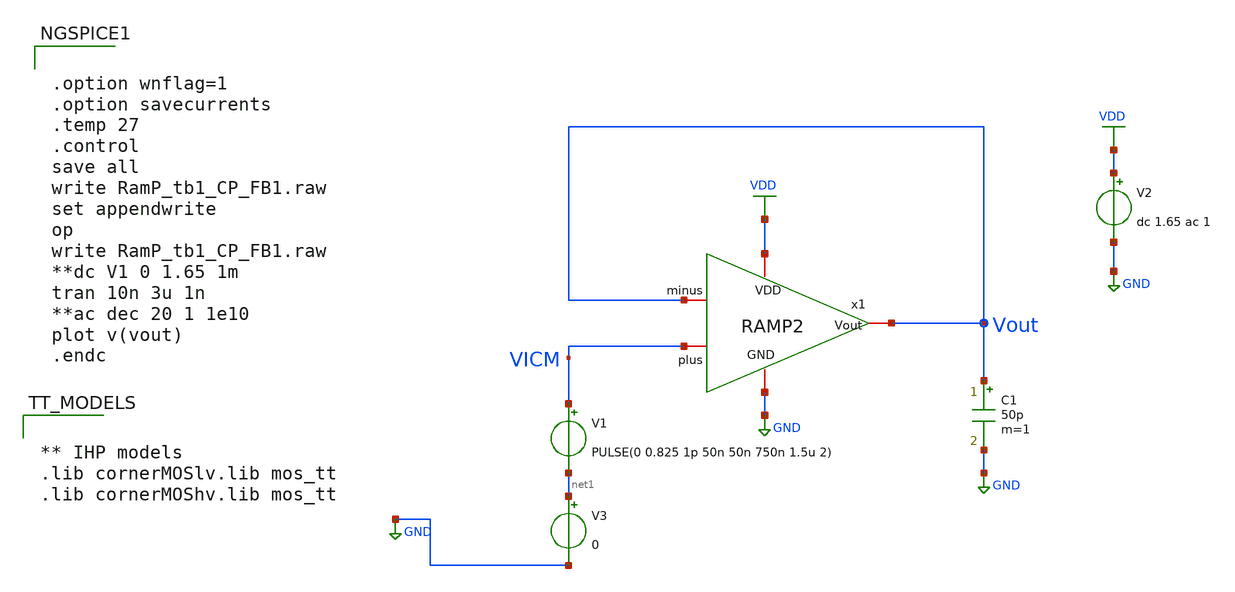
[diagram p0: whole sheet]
** sch_path: Design Files/RAMP/RAMP-Test/RamP_tb1_CP_FB1_1.sch
**.subckt RamP_tb1_CP_FB1_1
V2 VDD GND dc 1.65 ac 1
C1 Vout GND 50p m=1
x1 VDD VICM Vout Vout GND RAMP2
V1 VICM net1 PULSE(0 0.825 1p 50n 50n 750n 1.5u 2)
V3 net1 GND 0
**** begin user architecture code


** IHP models
.lib cornerMOSlv.lib mos_tt
.lib cornerMOShv.lib mos_tt




.save @n.x1.x2.xmn_stg2_3n1.nsg13_lv_nmos[gm]
.save @n.x1.x2.xmn_stg2_3n1.nsg13_lv_nmos[gds]
.save @n.x1.x2.xmn_stg2_3n1.nsg13_lv_nmos[vth]
.save @n.x1.x2.xmn_stg2_3n1.nsg13_lv_nmos[vdss]
.save @n.x1.x2.xmn_stg2_3n1.nsg13_lv_nmos[cgg]
.save @n.x1.x2.xmn_stg2_3n1.nsg13_lv_nmos[cgsol]
.save @n.x1.x2.xmn_stg2_3n1.nsg13_lv_nmos[cgdol]
.save @n.x1.x2.xmn_stg2_3p1.nsg13_lv_pmos[gm]
.save @n.x1.x2.xmn_stg2_3p1.nsg13_lv_pmos[gds]
.save @n.x1.x2.xmn_stg2_3p1.nsg13_lv_pmos[vth]
.save @n.x1.x2.xmn_stg2_3p1.nsg13_lv_pmos[vdss]
.save @n.x1.x2.xmn_stg2_3p1.nsg13_lv_pmos[cgg]
.save @n.x1.x2.xmn_stg2_3p1.nsg13_lv_pmos[cgsol]
.save @n.x1.x2.xmn_stg2_3p1.nsg13_lv_pmos[cgdol]
.save @n.x1.x2.xmp_dz_stg2_3n.nsg13_lv_pmos[gm]
.save @n.x1.x2.xmp_dz_stg2_3n.nsg13_lv_pmos[gds]
.save @n.x1.x2.xmp_dz_stg2_3n.nsg13_lv_pmos[vth]
.save @n.x1.x2.xmp_dz_stg2_3n.nsg13_lv_pmos[vdss]
.save @n.x1.x2.xmp_dz_stg2_3n.nsg13_lv_pmos[cgg]
.save @n.x1.x2.xmp_dz_stg2_3n.nsg13_lv_pmos[cgsol]
.save @n.x1.x2.xmp_dz_stg2_3n.nsg13_lv_pmos[cgdol]
.save @n.x1.x2.xmp_stg2_3p2.nsg13_lv_nmos[gm]
.save @n.x1.x2.xmp_stg2_3p2.nsg13_lv_nmos[gds]
.save @n.x1.x2.xmp_stg2_3p2.nsg13_lv_nmos[vth]
.save @n.x1.x2.xmp_stg2_3p2.nsg13_lv_nmos[vdss]
.save @n.x1.x2.xmp_stg2_3p2.nsg13_lv_nmos[cgg]
.save @n.x1.x2.xmp_stg2_3p2.nsg13_lv_nmos[cgsol]
.save @n.x1.x2.xmp_stg2_3p2.nsg13_lv_nmos[cgdol]
.save @n.x1.x2.xmp_stg2_3p1.nsg13_lv_pmos[gm]
.save @n.x1.x2.xmp_stg2_3p1.nsg13_lv_pmos[gds]
.save @n.x1.x2.xmp_stg2_3p1.nsg13_lv_pmos[vth]
.save @n.x1.x2.xmp_stg2_3p1.nsg13_lv_pmos[vdss]
.save @n.x1.x2.xmp_stg2_3p1.nsg13_lv_pmos[cgg]
.save @n.x1.x2.xmp_stg2_3p1.nsg13_lv_pmos[cgsol]
.save @n.x1.x2.xmp_stg2_3p1.nsg13_lv_pmos[cgdol]
.save @n.x1.x2.xmn_dz_stg2_3p.nsg13_lv_nmos[gm]
.save @n.x1.x2.xmn_dz_stg2_3p.nsg13_lv_nmos[gds]
.save @n.x1.x2.xmn_dz_stg2_3p.nsg13_lv_nmos[vth]
.save @n.x1.x2.xmn_dz_stg2_3p.nsg13_lv_nmos[vdss]
.save @n.x1.x2.xmn_dz_stg2_3p.nsg13_lv_nmos[cgg]
.save @n.x1.x2.xmn_dz_stg2_3p.nsg13_lv_nmos[cgsol]
.save @n.x1.x2.xmn_dz_stg2_3p.nsg13_lv_nmos[cgdol]
.save @n.x1.xm1.nsg13_hv_nmos[gm]
.save @n.x1.xm1.nsg13_hv_nmos[gds]
.save @n.x1.xm1.nsg13_hv_nmos[vth]
.save @n.x1.xm1.nsg13_hv_nmos[vdss]
.save @n.x1.xm1.nsg13_hv_nmos[cgg]
.save @n.x1.xm1.nsg13_hv_nmos[cgsol]
.save @n.x1.xm1.nsg13_hv_nmos[cgdol]
.save @n.x1.xm2.nsg13_hv_pmos[gm]
.save @n.x1.xm2.nsg13_hv_pmos[gds]
.save @n.x1.xm2.nsg13_hv_pmos[vth]
.save @n.x1.xm2.nsg13_hv_pmos[vdss]
.save @n.x1.xm2.nsg13_hv_pmos[cgg]
.save @n.x1.xm2.nsg13_hv_pmos[cgsol]
.save @n.x1.xm2.nsg13_hv_pmos[cgdol]
.save @n.x1.x3.xmn_stg2_3n1.nsg13_lv_nmos[gm]
.save @n.x1.x3.xmn_stg2_3n1.nsg13_lv_nmos[gds]
.save @n.x1.x3.xmn_stg2_3n1.nsg13_lv_nmos[vth]
.save @n.x1.x3.xmn_stg2_3n1.nsg13_lv_nmos[vdss]
.save @n.x1.x3.xmn_stg2_3n1.nsg13_lv_nmos[cgg]
.save @n.x1.x3.xmn_stg2_3n1.nsg13_lv_nmos[cgsol]
.save @n.x1.x3.xmn_stg2_3n1.nsg13_lv_nmos[cgdol]
.save @n.x1.x3.xmn_stg2_3p1.nsg13_lv_pmos[gm]
.save @n.x1.x3.xmn_stg2_3p1.nsg13_lv_pmos[gds]
.save @n.x1.x3.xmn_stg2_3p1.nsg13_lv_pmos[vth]
.save @n.x1.x3.xmn_stg2_3p1.nsg13_lv_pmos[vdss]
.save @n.x1.x3.xmn_stg2_3p1.nsg13_lv_pmos[cgg]
.save @n.x1.x3.xmn_stg2_3p1.nsg13_lv_pmos[cgsol]
.save @n.x1.x3.xmn_stg2_3p1.nsg13_lv_pmos[cgdol]
.save @n.x1.x3.xmp_dz_stg2_3n.nsg13_lv_pmos[gm]
.save @n.x1.x3.xmp_dz_stg2_3n.nsg13_lv_pmos[gds]
.save @n.x1.x3.xmp_dz_stg2_3n.nsg13_lv_pmos[vth]
.save @n.x1.x3.xmp_dz_stg2_3n.nsg13_lv_pmos[vdss]
.save @n.x1.x3.xmp_dz_stg2_3n.nsg13_lv_pmos[cgg]
.save @n.x1.x3.xmp_dz_stg2_3n.nsg13_lv_pmos[cgsol]
.save @n.x1.x3.xmp_dz_stg2_3n.nsg13_lv_pmos[cgdol]
.save @n.x1.x3.xmp_stg2_3p2.nsg13_lv_nmos[gm]
.save @n.x1.x3.xmp_stg2_3p2.nsg13_lv_nmos[gds]
.save @n.x1.x3.xmp_stg2_3p2.nsg13_lv_nmos[vth]
.save @n.x1.x3.xmp_stg2_3p2.nsg13_lv_nmos[vdss]
.save @n.x1.x3.xmp_stg2_3p2.nsg13_lv_nmos[cgg]
.save @n.x1.x3.xmp_stg2_3p2.nsg13_lv_nmos[cgsol]
.save @n.x1.x3.xmp_stg2_3p2.nsg13_lv_nmos[cgdol]
.save @n.x1.x3.xmp_stg2_3p1.nsg13_lv_pmos[gm]
.save @n.x1.x3.xmp_stg2_3p1.nsg13_lv_pmos[gds]
.save @n.x1.x3.xmp_stg2_3p1.nsg13_lv_pmos[vth]
.save @n.x1.x3.xmp_stg2_3p1.nsg13_lv_pmos[vdss]
.save @n.x1.x3.xmp_stg2_3p1.nsg13_lv_pmos[cgg]
.save @n.x1.x3.xmp_stg2_3p1.nsg13_lv_pmos[cgsol]
.save @n.x1.x3.xmp_stg2_3p1.nsg13_lv_pmos[cgdol]
.save @n.x1.x3.xmn_dz_stg2_3p.nsg13_lv_nmos[gm]
.save @n.x1.x3.xmn_dz_stg2_3p.nsg13_lv_nmos[gds]
.save @n.x1.x3.xmn_dz_stg2_3p.nsg13_lv_nmos[vth]
.save @n.x1.x3.xmn_dz_stg2_3p.nsg13_lv_nmos[vdss]
.save @n.x1.x3.xmn_dz_stg2_3p.nsg13_lv_nmos[cgg]
.save @n.x1.x3.xmn_dz_stg2_3p.nsg13_lv_nmos[cgsol]
.save @n.x1.x3.xmn_dz_stg2_3p.nsg13_lv_nmos[cgdol]
.save @n.x1.x3.xmn_stg2_3n_r.nsg13_hv_nmos[gm]
.save @n.x1.x3.xmn_stg2_3n_r.nsg13_hv_nmos[gds]
.save @n.x1.x3.xmn_stg2_3n_r.nsg13_hv_nmos[vth]
.save @n.x1.x3.xmn_stg2_3n_r.nsg13_hv_nmos[vdss]
.save @n.x1.x3.xmn_stg2_3n_r.nsg13_hv_nmos[cgg]
.save @n.x1.x3.xmn_stg2_3n_r.nsg13_hv_nmos[cgsol]
.save @n.x1.x3.xmn_stg2_3n_r.nsg13_hv_nmos[cgdol]
.save @n.x1.x3.x1.xm2.nsg13_lv_pmos[gm]
.save @n.x1.x3.x1.xm2.nsg13_lv_pmos[gds]
.save @n.x1.x3.x1.xm2.nsg13_lv_pmos[vth]
.save @n.x1.x3.x1.xm2.nsg13_lv_pmos[vdss]
.save @n.x1.x3.x1.xm2.nsg13_lv_pmos[cgg]
.save @n.x1.x3.x1.xm2.nsg13_lv_pmos[cgsol]
.save @n.x1.x3.x1.xm2.nsg13_lv_pmos[cgdol]
.save @n.x1.x3.x1.xm4.nsg13_hv_nmos[gm]
.save @n.x1.x3.x1.xm4.nsg13_hv_nmos[gds]
.save @n.x1.x3.x1.xm4.nsg13_hv_nmos[vth]
.save @n.x1.x3.x1.xm4.nsg13_hv_nmos[vdss]
.save @n.x1.x3.x1.xm4.nsg13_hv_nmos[cgg]
.save @n.x1.x3.x1.xm4.nsg13_hv_nmos[cgsol]
.save @n.x1.x3.x1.xm4.nsg13_hv_nmos[cgdol]
.save @n.x1.x3.x1.xm5.nsg13_hv_nmos[gm]
.save @n.x1.x3.x1.xm5.nsg13_hv_nmos[gds]
.save @n.x1.x3.x1.xm5.nsg13_hv_nmos[vth]
.save @n.x1.x3.x1.xm5.nsg13_hv_nmos[vdss]
.save @n.x1.x3.x1.xm5.nsg13_hv_nmos[cgg]
.save @n.x1.x3.x1.xm5.nsg13_hv_nmos[cgsol]
.save @n.x1.x3.x1.xm5.nsg13_hv_nmos[cgdol]
.save @n.x1.x3.x1.xm1.nsg13_lv_pmos[gm]
.save @n.x1.x3.x1.xm1.nsg13_lv_pmos[gds]
.save @n.x1.x3.x1.xm1.nsg13_lv_pmos[vth]
.save @n.x1.x3.x1.xm1.nsg13_lv_pmos[vdss]
.save @n.x1.x3.x1.xm1.nsg13_lv_pmos[cgg]
.save @n.x1.x3.x1.xm1.nsg13_lv_pmos[cgsol]
.save @n.x1.x3.x1.xm1.nsg13_lv_pmos[cgdol]
.save @n.x1.x3.xmp_stg2_3p_r.nsg13_hv_pmos[gm]
.save @n.x1.x3.xmp_stg2_3p_r.nsg13_hv_pmos[gds]
.save @n.x1.x3.xmp_stg2_3p_r.nsg13_hv_pmos[vth]
.save @n.x1.x3.xmp_stg2_3p_r.nsg13_hv_pmos[vdss]
.save @n.x1.x3.xmp_stg2_3p_r.nsg13_hv_pmos[cgg]
.save @n.x1.x3.xmp_stg2_3p_r.nsg13_hv_pmos[cgsol]
.save @n.x1.x3.xmp_stg2_3p_r.nsg13_hv_pmos[cgdol]
.save @n.x1.x3.x2.xm1.nsg13_hv_nmos[gm]
.save @n.x1.x3.x2.xm1.nsg13_hv_nmos[gds]
.save @n.x1.x3.x2.xm1.nsg13_hv_nmos[vth]
.save @n.x1.x3.x2.xm1.nsg13_hv_nmos[vdss]
.save @n.x1.x3.x2.xm1.nsg13_hv_nmos[cgg]
.save @n.x1.x3.x2.xm1.nsg13_hv_nmos[cgsol]
.save @n.x1.x3.x2.xm1.nsg13_hv_nmos[cgdol]
.save @n.x1.x3.x2.xm2.nsg13_hv_nmos[gm]
.save @n.x1.x3.x2.xm2.nsg13_hv_nmos[gds]
.save @n.x1.x3.x2.xm2.nsg13_hv_nmos[vth]
.save @n.x1.x3.x2.xm2.nsg13_hv_nmos[vdss]
.save @n.x1.x3.x2.xm2.nsg13_hv_nmos[cgg]
.save @n.x1.x3.x2.xm2.nsg13_hv_nmos[cgsol]
.save @n.x1.x3.x2.xm2.nsg13_hv_nmos[cgdol]
.save @n.x1.x3.x2.xm3.nsg13_hv_pmos[gm]
.save @n.x1.x3.x2.xm3.nsg13_hv_pmos[gds]
.save @n.x1.x3.x2.xm3.nsg13_hv_pmos[vth]
.save @n.x1.x3.x2.xm3.nsg13_hv_pmos[vdss]
.save @n.x1.x3.x2.xm3.nsg13_hv_pmos[cgg]
.save @n.x1.x3.x2.xm3.nsg13_hv_pmos[cgsol]
.save @n.x1.x3.x2.xm3.nsg13_hv_pmos[cgdol]
.save @n.x1.x3.x2.xm4.nsg13_hv_pmos[gm]
.save @n.x1.x3.x2.xm4.nsg13_hv_pmos[gds]
.save @n.x1.x3.x2.xm4.nsg13_hv_pmos[vth]
.save @n.x1.x3.x2.xm4.nsg13_hv_pmos[vdss]
.save @n.x1.x3.x2.xm4.nsg13_hv_pmos[cgg]
.save @n.x1.x3.x2.xm4.nsg13_hv_pmos[cgsol]
.save @n.x1.x3.x2.xm4.nsg13_hv_pmos[cgdol]
.save @n.x1.x4.xm9.nsg13_lv_nmos[gm]
.save @n.x1.x4.xm9.nsg13_lv_nmos[gds]
.save @n.x1.x4.xm9.nsg13_lv_nmos[vth]
.save @n.x1.x4.xm9.nsg13_lv_nmos[vdss]
.save @n.x1.x4.xm9.nsg13_lv_nmos[cgg]
.save @n.x1.x4.xm9.nsg13_lv_nmos[cgsol]
.save @n.x1.x4.xm9.nsg13_lv_nmos[cgdol]
.save @n.x1.x4.xm10.nsg13_lv_pmos[gm]
.save @n.x1.x4.xm10.nsg13_lv_pmos[gds]
.save @n.x1.x4.xm10.nsg13_lv_pmos[vth]
.save @n.x1.x4.xm10.nsg13_lv_pmos[vdss]
.save @n.x1.x4.xm10.nsg13_lv_pmos[cgg]
.save @n.x1.x4.xm10.nsg13_lv_pmos[cgsol]
.save @n.x1.x4.xm10.nsg13_lv_pmos[cgdol]
.save @n.x1.x4.xm11.nsg13_lv_pmos[gm]
.save @n.x1.x4.xm11.nsg13_lv_pmos[gds]
.save @n.x1.x4.xm11.nsg13_lv_pmos[vth]
.save @n.x1.x4.xm11.nsg13_lv_pmos[vdss]
.save @n.x1.x4.xm11.nsg13_lv_pmos[cgg]
.save @n.x1.x4.xm11.nsg13_lv_pmos[cgsol]
.save @n.x1.x4.xm11.nsg13_lv_pmos[cgdol]
.save @n.x1.x4.xm12.nsg13_lv_nmos[gm]
.save @n.x1.x4.xm12.nsg13_lv_nmos[gds]
.save @n.x1.x4.xm12.nsg13_lv_nmos[vth]
.save @n.x1.x4.xm12.nsg13_lv_nmos[vdss]
.save @n.x1.x4.xm12.nsg13_lv_nmos[cgg]
.save @n.x1.x4.xm12.nsg13_lv_nmos[cgsol]
.save @n.x1.x4.xm12.nsg13_lv_nmos[cgdol]
.save @n.x1.x4.xm13.nsg13_lv_pmos[gm]
.save @n.x1.x4.xm13.nsg13_lv_pmos[gds]
.save @n.x1.x4.xm13.nsg13_lv_pmos[vth]
.save @n.x1.x4.xm13.nsg13_lv_pmos[vdss]
.save @n.x1.x4.xm13.nsg13_lv_pmos[cgg]
.save @n.x1.x4.xm13.nsg13_lv_pmos[cgsol]
.save @n.x1.x4.xm13.nsg13_lv_pmos[cgdol]
.save @n.x1.x4.xm14.nsg13_lv_nmos[gm]
.save @n.x1.x4.xm14.nsg13_lv_nmos[gds]
.save @n.x1.x4.xm14.nsg13_lv_nmos[vth]
.save @n.x1.x4.xm14.nsg13_lv_nmos[vdss]
.save @n.x1.x4.xm14.nsg13_lv_nmos[cgg]
.save @n.x1.x4.xm14.nsg13_lv_nmos[cgsol]
.save @n.x1.x4.xm14.nsg13_lv_nmos[cgdol]
.save @n.x1.x5.xmn_stg1_ip_n1.nsg13_lv_nmos[gm]
.save @n.x1.x5.xmn_stg1_ip_n1.nsg13_lv_nmos[gds]
.save @n.x1.x5.xmn_stg1_ip_n1.nsg13_lv_nmos[vth]
.save @n.x1.x5.xmn_stg1_ip_n1.nsg13_lv_nmos[vdss]
.save @n.x1.x5.xmn_stg1_ip_n1.nsg13_lv_nmos[cgg]
.save @n.x1.x5.xmn_stg1_ip_n1.nsg13_lv_nmos[cgsol]
.save @n.x1.x5.xmn_stg1_ip_n1.nsg13_lv_nmos[cgdol]
.save @n.x1.x5.xmn_stg1_ip_n2.nsg13_lv_nmos[gm]
.save @n.x1.x5.xmn_stg1_ip_n2.nsg13_lv_nmos[gds]
.save @n.x1.x5.xmn_stg1_ip_n2.nsg13_lv_nmos[vth]
.save @n.x1.x5.xmn_stg1_ip_n2.nsg13_lv_nmos[vdss]
.save @n.x1.x5.xmn_stg1_ip_n2.nsg13_lv_nmos[cgg]
.save @n.x1.x5.xmn_stg1_ip_n2.nsg13_lv_nmos[cgsol]
.save @n.x1.x5.xmn_stg1_ip_n2.nsg13_lv_nmos[cgdol]
.save @n.x1.x5.xmp_stg1_cl_p1.nsg13_hv_pmos[gm]
.save @n.x1.x5.xmp_stg1_cl_p1.nsg13_hv_pmos[gds]
.save @n.x1.x5.xmp_stg1_cl_p1.nsg13_hv_pmos[vth]
.save @n.x1.x5.xmp_stg1_cl_p1.nsg13_hv_pmos[vdss]
.save @n.x1.x5.xmp_stg1_cl_p1.nsg13_hv_pmos[cgg]
.save @n.x1.x5.xmp_stg1_cl_p1.nsg13_hv_pmos[cgsol]
.save @n.x1.x5.xmp_stg1_cl_p1.nsg13_hv_pmos[cgdol]
.save @n.x1.x5.xmp_stg1_cl_p2.nsg13_hv_pmos[gm]
.save @n.x1.x5.xmp_stg1_cl_p2.nsg13_hv_pmos[gds]
.save @n.x1.x5.xmp_stg1_cl_p2.nsg13_hv_pmos[vth]
.save @n.x1.x5.xmp_stg1_cl_p2.nsg13_hv_pmos[vdss]
.save @n.x1.x5.xmp_stg1_cl_p2.nsg13_hv_pmos[cgg]
.save @n.x1.x5.xmp_stg1_cl_p2.nsg13_hv_pmos[cgsol]
.save @n.x1.x5.xmp_stg1_cl_p2.nsg13_hv_pmos[cgdol]



.option wnflag=1
.option savecurrents
.temp 27
.control
save all
write RamP_tb1_CP_FB1.raw
set appendwrite
op
write RamP_tb1_CP_FB1.raw
**dc V1 0 1.65 1m
tran 10n 3u 1n
**ac dec 20 1 1e10
plot v(vout)
.endc


**** end user architecture code
**.ends

* expanding   symbol:  /foss/designs/RAMP/Fully-Diff-RAMP/RAMP2.sym # of pins=5
** sym_path: Design Files/RAMP/Fully-Diff-RAMP/RAMP2.sym
** sch_path: Design Files/RAMP/Fully-Diff-RAMP/RAMP2.sch
.subckt RAMP2 VDD plus Vout minus GND
*.iopin GND
*.iopin plus
*.iopin minus
*.iopin Vout
*.iopin VDD
x2 VDD net2 mp_dz Vo_STG1 mn_dz net1 GND STG2
XM1 Vout mn_dz GND GND sg13_hv_nmos w=2.3u l=1u ng=1 m=4 mm_ok=1
XM2 Vout mp_dz VDD VDD sg13_hv_pmos w=4.5u l=0.5u ng=1 m=4 mm_ok=1
x3 VDD net2 V1_CM net1 GND STG2_Replica
x4 VDD V1_CM GND STG1-CM
x5 VDD Vo_STG1 plus minus V1_CM GND STG1_2
.ends


* expanding   symbol:  Fully-Diff-RAMP/STG2.sym # of pins=7
** sym_path: Design Files/RAMP/Fully-Diff-RAMP/STG2.sym
** sch_path: Design Files/RAMP/Fully-Diff-RAMP/STG2.sch
.subckt STG2 VDD VCTRL_P VDZP Vin_2 VDZN VCTRL_N GND
*.ipin Vin_2
*.ipin VDD
*.ipin GND
*.ipin VCTRL_P
*.ipin VCTRL_N
*.opin VDZN
*.opin VDZP
XMN_STG2_3N1 VDZN Vin_2 GND GND sg13_lv_nmos w=0.15u l=0.13u ng=1 m=1 mm_ok=1
XMN_STG2_3P1 VDZN Vin_2 net1 VDD sg13_lv_pmos w=0.15u l=0.13u ng=1 m=3 mm_ok=1
XMP_DZ_STG2_3N net1 VCTRL_P VDD VDD sg13_lv_pmos w=0.15u l=0.13u ng=1 m=5 mm_ok=1
XMP_STG2_3P2 VDZP Vin_2 net2 net2 sg13_lv_nmos w=0.15u l=0.13u ng=1 m=1 mm_ok=1
XMP_STG2_3P1 VDZP Vin_2 VDD VDD sg13_lv_pmos w=0.15u l=0.13u ng=1 m=1 mm_ok=1
XMN_DZ_STG2_3P net2 VCTRL_N GND GND sg13_lv_nmos w=0.15u l=0.13u ng=1 m=1 mm_ok=1
.ends


* expanding   symbol:  Fully-Diff-RAMP/STG2_Replica.sym # of pins=5
** sym_path: Design Files/RAMP/Fully-Diff-RAMP/STG2_Replica.sym
** sch_path: Design Files/RAMP/Fully-Diff-RAMP/STG2_Replica.sch
.subckt STG2_Replica VDD VCTRLP Vin_STG2 VCTRLN GND
*.ipin Vin_STG2
*.iopin VDD
*.iopin GND
*.opin VCTRLP
*.opin VCTRLN
XMN_STG2_3N1 net1 Vin_STG2 GND GND sg13_lv_nmos w=0.15u l=0.13u ng=1 m=1 mm_ok=1
XMN_STG2_3P1 net1 Vin_STG2 net2 VDD sg13_lv_pmos w=0.15u l=0.13u ng=1 m=3 mm_ok=1
XMP_DZ_STG2_3N net2 VCTRLP VDD VDD sg13_lv_pmos w=0.15u l=0.13u ng=1 m=5 mm_ok=1
XMP_STG2_3P2 net4 Vin_STG2 net3 net3 sg13_lv_nmos w=0.15u l=0.13u ng=1 m=1 mm_ok=1
XMP_STG2_3P1 net4 Vin_STG2 VDD VDD sg13_lv_pmos w=0.15u l=0.13u ng=1 m=1 mm_ok=1
XMN_DZ_STG2_3P net3 VCTRLN GND GND sg13_lv_nmos w=0.15u l=0.13u ng=1 m=1 mm_ok=1
XMN_STG2_3N_R net5 net5 GND GND sg13_hv_nmos w=2.3u l=1u ng=1 m=1 mm_ok=1
I0 VDD net5 1u
x1 VDD net1 net5 VCTRLP GND POTA
XMP_STG2_3P_R net6 net6 VDD VDD sg13_hv_pmos w=4.5u l=0.5u ng=1 m=1 mm_ok=1
I1 net6 GND 1u
x2 VDD VCTRLN net4 net6 GND NOTA
.ends


* expanding   symbol:  Fully-Diff-RAMP/STG1-CM.sym # of pins=3
** sym_path: Design Files/RAMP/Fully-Diff-RAMP/STG1-CM.sym
** sch_path: Design Files/RAMP/Fully-Diff-RAMP/STG1-CM.sch
.subckt STG1-CM VDD V_CM1 GND
*.ipin VDD
*.ipin GND
*.opin V_CM1
XM9 V_CM1 V_CM1 GND GND sg13_lv_nmos w=0.15u l=0.13u ng=1 m=1 mm_ok=1
XM10 V_CM1 V_CM1 net1 VDD sg13_lv_pmos w=0.15u l=0.13u ng=1 m=3 mm_ok=1
XM11 net1 GND VDD VDD sg13_lv_pmos w=0.15u l=0.13u ng=1 m=5 mm_ok=1
XM12 V_CM1 V_CM1 net2 net2 sg13_lv_nmos w=0.15u l=0.13u ng=1 m=1 mm_ok=1
XM13 V_CM1 V_CM1 VDD VDD sg13_lv_pmos w=0.15u l=0.13u ng=1 m=1 mm_ok=1
XM14 net2 VDD GND GND sg13_lv_nmos w=0.15u l=0.13u ng=1 m=1 mm_ok=1
.ends


* expanding   symbol:  Fully-Diff-RAMP/STG1_2.sym # of pins=6
** sym_path: Design Files/RAMP/Fully-Diff-RAMP/STG1_2.sym
** sch_path: Design Files/RAMP/Fully-Diff-RAMP/STG1_2.sch
.subckt STG1_2 VDD Vo1 Vip Vin V1_CM GND
*.iopin VDD
*.iopin GND
*.opin Vo1
*.ipin Vip
*.ipin Vin
*.ipin V1_CM
R1 VR net2 100k m=1
R3 VR Vo1 100k m=1
XMN_STG1_IP_N1 net2 Vip net3 GND sg13_lv_nmos w=1.563u l=0.5u ng=1 m=2 mm_ok=1
XMN_STG1_IP_N2 Vo1 Vin net3 GND sg13_lv_nmos w=1.563u l=0.5u ng=1 m=2 mm_ok=1
I0 net3 GND 10u
XMP_STG1_CL_P1 net2 net1 VDD VDD sg13_hv_pmos w=0.5u l=1u ng=1 m=1 mm_ok=1
XMP_STG1_CL_P2 Vo1 net1 VDD VDD sg13_hv_pmos w=0.5u l=1u ng=1 m=1 mm_ok=1
B2 net1 GND V = 1.8 / ( 1 + exp(-10000 * V(VR,V1_CM)))
.ends


* expanding   symbol:  OTA/POTA.sym # of pins=5
** sym_path: Design Files/RAMP/OTA/POTA.sym
** sch_path: Design Files/RAMP/OTA/POTA.sch
.subckt POTA VDD PLUS MINUS Vout GND
*.ipin VDD
*.ipin GND
*.ipin PLUS
*.ipin MINUS
*.opin Vout
XM2 net2 PLUS net1 VDD sg13_lv_pmos w=1.2u l=0.5u ng=1 m=2 mm_ok=1
XM3 Vout MINUS net1 VDD sg13_lv_pmos w=1.2u l=0.5u ng=1 m=2 mm_ok=1
XM4 Vout net2 GND GND sg13_hv_nmos w=0.5u l=2u ng=1 m=1 mm_ok=1
XM5 net2 net2 GND GND sg13_hv_nmos w=0.5u l=2u ng=1 m=1 mm_ok=1
I1 VDD net1 2u
.ends


* expanding   symbol:  OTA/NOTA.sym # of pins=5
** sym_path: Design Files/RAMP/OTA/NOTA.sym
** sch_path: Design Files/RAMP/OTA/NOTA.sch
.subckt NOTA VDD Vout PLUS MINUS GND
*.ipin VDD
*.ipin GND
*.ipin PLUS
*.ipin MINUS
*.opin Vout
XM1 net2 PLUS net1 GND sg13_hv_nmos w=1.75u l=1u ng=1 m=2 mm_ok=1
XM2 Vout MINUS net1 GND sg13_hv_nmos w=1.75u l=1u ng=1 m=2 mm_ok=1
I0 net1 GND 2u
XM3 Vout net2 VDD VDD sg13_hv_pmos w=0.5u l=0.75u ng=1 m=1 mm_ok=1
XM4 net2 net2 VDD VDD sg13_hv_pmos w=0.5u l=0.75u ng=1 m=1 mm_ok=1
.ends

.GLOBAL VDD
.GLOBAL GND
.end
